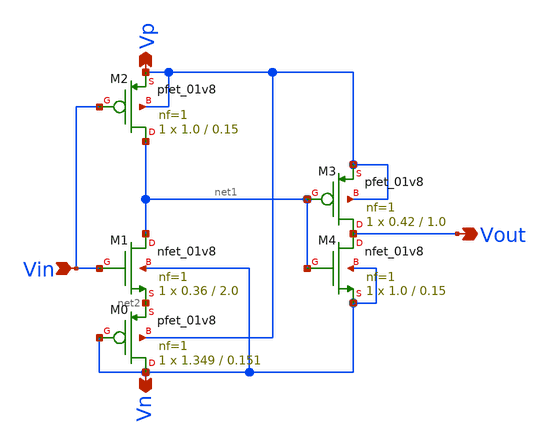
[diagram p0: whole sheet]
** sch_path: xschem/Vth_sch/Symbol/th12.sch
**.subckt th12 Vn Vp Vin Vout
*.opin Vn
*.opin Vp
*.ipin Vin
*.opin Vout
XM3 Vout net1 Vp Vp sky130_fd_pr__pfet_01v8 L=1.0 W=0.42 nf=1 ad='int((nf+1)/2) * W/nf * 0.29' as='int((nf+2)/2) * W/nf * 0.29'
+ pd='2*int((nf+1)/2) * (W/nf + 0.29)' ps='2*int((nf+2)/2) * (W/nf + 0.29)' nrd='0.29 / W' nrs='0.29 / W'
+ sa=0 sb=0 sd=0 mult=1 m=1
XM4 Vout net1 Vn Vn sky130_fd_pr__nfet_01v8 L=0.15 W=1.0 nf=1 ad='int((nf+1)/2) * W/nf * 0.29' as='int((nf+2)/2) * W/nf * 0.29'
+ pd='2*int((nf+1)/2) * (W/nf + 0.29)' ps='2*int((nf+2)/2) * (W/nf + 0.29)' nrd='0.29 / W' nrs='0.29 / W'
+ sa=0 sb=0 sd=0 mult=1 m=1
XM2 net1 Vin Vp Vp sky130_fd_pr__pfet_01v8 L=0.15 W=1.0 nf=1 ad='int((nf+1)/2) * W/nf * 0.29' as='int((nf+2)/2) * W/nf * 0.29'
+ pd='2*int((nf+1)/2) * (W/nf + 0.29)' ps='2*int((nf+2)/2) * (W/nf + 0.29)' nrd='0.29 / W' nrs='0.29 / W'
+ sa=0 sb=0 sd=0 mult=1 m=1
XM1 net1 Vin net2 Vn sky130_fd_pr__nfet_01v8 L=2.0 W=0.36 nf=1 ad='int((nf+1)/2) * W/nf * 0.29' as='int((nf+2)/2) * W/nf * 0.29'
+ pd='2*int((nf+1)/2) * (W/nf + 0.29)' ps='2*int((nf+2)/2) * (W/nf + 0.29)' nrd='0.29 / W' nrs='0.29 / W'
+ sa=0 sb=0 sd=0 mult=1 m=1
XM0 Vn Vn net2 Vp sky130_fd_pr__pfet_01v8 L=0.151 W=1.349 nf=1 ad='int((nf+1)/2) * W/nf * 0.29' as='int((nf+2)/2) * W/nf * 0.29'
+ pd='2*int((nf+1)/2) * (W/nf + 0.29)' ps='2*int((nf+2)/2) * (W/nf + 0.29)' nrd='0.29 / W' nrs='0.29 / W'
+ sa=0 sb=0 sd=0 mult=1 m=1
**.ends
.end
